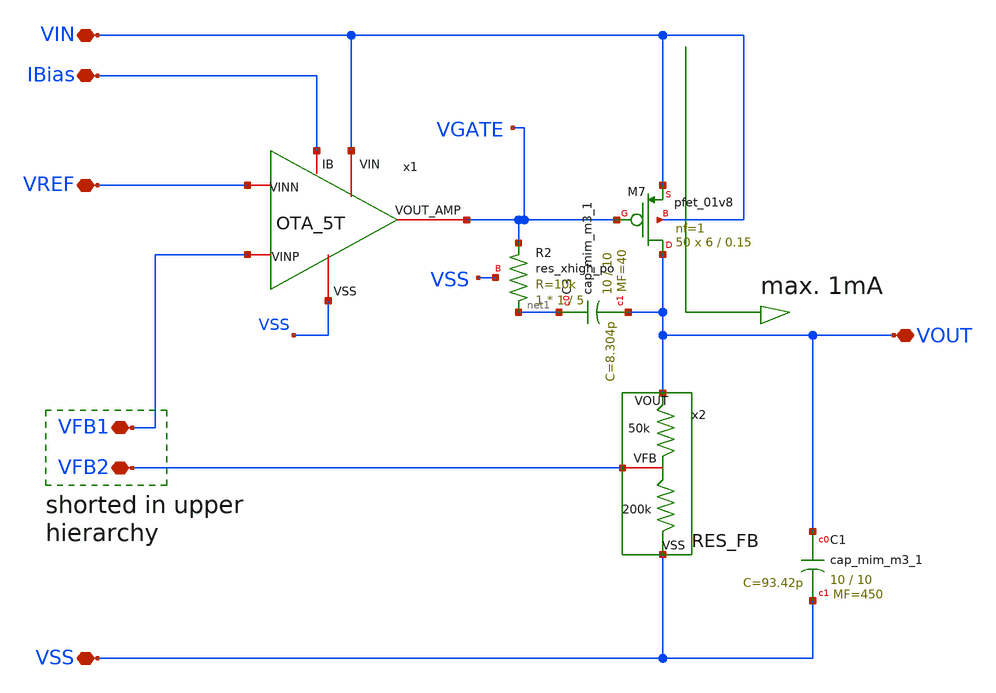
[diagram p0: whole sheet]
** sch_path: LDO_1p5V/schematics/LDO.sch
**.subckt LDO VIN VREF VFB1 VSS VFB2 VOUT IBias
*.iopin VIN
*.iopin VREF
*.iopin VFB1
*.iopin VSS
*.iopin VFB2
*.iopin VOUT
*.iopin IBias
x2 VOUT VFB2 VSS RES_FB
x1 VIN VGATE VREF VFB1 IBias VSS OTA_5T
XC3 net1 VOUT sky130_fd_pr__cap_mim_m3_1 W=10 L=10 MF=40 m=40
XM7 VOUT VGATE VIN VIN sky130_fd_pr__pfet_01v8 L=0.15 W=6 nf=1 ad='int((1 + 1)/2) * 6 / 1 * 0.29' as='int((1 + 2)/2) * 6 / 1 * 0.29'
+ pd='2*int((1 + 1)/2) * (6 / 1 + 0.29)' ps='2*int((1 + 2)/2) * (6 / 1 + 0.29)' nrd='0.29 / 6 ' nrs='0.29 / 6 '
+ sa=0 sb=0 sd=0 mult=50 m=50
XC1 VOUT VSS sky130_fd_pr__cap_mim_m3_1 W=10 L=10 MF=450 m=450
XR2 net1 VGATE VSS sky130_fd_pr__res_xhigh_po W=1 L=5 mult=1 m=1
**.ends

* expanding   symbol:  /foss/designs/IPN/LDO_1p5V/schematics/RES_FB.sym # of pins=3
** sym_path: RES_FB/RES_FB.sym
** sch_path: RES_FB/RES_FB.sch
.subckt RES_FB VOUT VFB VSS
*.iopin VOUT
*.iopin VFB
*.iopin VSS
XR11 net1 VOUT VSS sky130_fd_pr__res_xhigh_po_0p69 L=8.62 mult=1 m=1
XR1 VFB net1 VSS sky130_fd_pr__res_xhigh_po_0p69 L=8.62 mult=1 m=1
XR2 net8 VFB VSS sky130_fd_pr__res_xhigh_po_0p69 L=8.62 mult=1 m=1
XR3 net4 net8 VSS sky130_fd_pr__res_xhigh_po_0p69 L=8.62 mult=1 m=1
XR4 net2 net4 VSS sky130_fd_pr__res_xhigh_po_0p69 L=8.62 mult=1 m=1
XR5 net5 net2 VSS sky130_fd_pr__res_xhigh_po_0p69 L=8.62 mult=1 m=1
XR6 net3 net5 VSS sky130_fd_pr__res_xhigh_po_0p69 L=8.62 mult=1 m=1
XR7 net7 net3 VSS sky130_fd_pr__res_xhigh_po_0p69 L=8.62 mult=1 m=1
XR8 net6 net7 VSS sky130_fd_pr__res_xhigh_po_0p69 L=8.62 mult=1 m=1
XR9 VSS net6 VSS sky130_fd_pr__res_xhigh_po_0p69 L=8.62 mult=1 m=1
.ends


* expanding   symbol:  /foss/designs/IPN/LDO_1p5V/schematics/OTA_5T.sym # of pins=6
** sym_path: /foss/designs/IPN/LDO_1p5V/schematics/OTA_5T.sym
** sch_path: /foss/designs/IPN/LDO_1p5V/schematics/OTA_5T.sch
.subckt OTA_5T VIN VOUT_AMP VINN VINP IB VSS
*.iopin VIN
*.iopin VSS
*.iopin VOUT_AMP
*.iopin IB
*.iopin VINN
*.iopin VINP
XM1 IB IB VSS VSS sky130_fd_pr__nfet_01v8 L=1 W=2.5 nf=1 ad='int((1 + 1)/2) * 2.5 / 1 * 0.29' as='int((1 + 2)/2) * 2.5 / 1 * 0.29'
+ pd='2*int((1 + 1)/2) * (2.5 / 1 + 0.29)' ps='2*int((1 + 2)/2) * (2.5 / 1 + 0.29)' nrd='0.29 / 2.5 ' nrs='0.29 / 2.5 '
+ sa=0 sb=0 sd=0 mult=4 m=4
XM2 tail IB VSS VSS sky130_fd_pr__nfet_01v8 L=1 W=2.5 nf=1 ad='int((1 + 1)/2) * 2.5 / 1 * 0.29' as='int((1 + 2)/2) * 2.5 / 1 * 0.29'
+ pd='2*int((1 + 1)/2) * (2.5 / 1 + 0.29)' ps='2*int((1 + 2)/2) * (2.5 / 1 + 0.29)' nrd='0.29 / 2.5 ' nrs='0.29 / 2.5 '
+ sa=0 sb=0 sd=0 mult=4 m=4
XM5 VOUT_AMP net1 VIN VIN sky130_fd_pr__pfet_01v8 L=1 W=6 nf=1 ad='int((1 + 1)/2) * 6 / 1 * 0.29' as='int((1 + 2)/2) * 6 / 1 * 0.29'
+ pd='2*int((1 + 1)/2) * (6 / 1 + 0.29)' ps='2*int((1 + 2)/2) * (6 / 1 + 0.29)' nrd='0.29 / 6 ' nrs='0.29 / 6 '
+ sa=0 sb=0 sd=0 mult=4 m=4
XM6 net1 net1 VIN VIN sky130_fd_pr__pfet_01v8 L=1 W=6 nf=1 ad='int((1 + 1)/2) * 6 / 1 * 0.29' as='int((1 + 2)/2) * 6 / 1 * 0.29'
+ pd='2*int((1 + 1)/2) * (6 / 1 + 0.29)' ps='2*int((1 + 2)/2) * (6 / 1 + 0.29)' nrd='0.29 / 6 ' nrs='0.29 / 6 '
+ sa=0 sb=0 sd=0 mult=4 m=4
XD tail VSS tail VSS sky130_fd_pr__nfet_01v8 L=0.15 W=3 nf=1 ad='int((1 + 1)/2) * 3 / 1 * 0.29' as='int((1 + 2)/2) * 3 / 1 * 0.29'
+ pd='2*int((1 + 1)/2) * (3 / 1 + 0.29)' ps='2*int((1 + 2)/2) * (3 / 1 + 0.29)' nrd='0.29 / 3 ' nrs='0.29 / 3 '
+ sa=0 sb=0 sd=0 mult=4 m=4
XM7 VIN VIN VIN VIN sky130_fd_pr__pfet_01v8 L=0.15 W=6 nf=1 ad='int((1 + 1)/2) * 6 / 1 * 0.29' as='int((1 + 2)/2) * 6 / 1 * 0.29'
+ pd='2*int((1 + 1)/2) * (6 / 1 + 0.29)' ps='2*int((1 + 2)/2) * (6 / 1 + 0.29)' nrd='0.29 / 6 ' nrs='0.29 / 6 '
+ sa=0 sb=0 sd=0 mult=4 m=4
XM3 net1 VINP tail VSS sky130_fd_pr__nfet_01v8 L=1 W=3 nf=1 ad='int((1 + 1)/2) * 3 / 1 * 0.29' as='int((1 + 2)/2) * 3 / 1 * 0.29'
+ pd='2*int((1 + 1)/2) * (3 / 1 + 0.29)' ps='2*int((1 + 2)/2) * (3 / 1 + 0.29)' nrd='0.29 / 3 ' nrs='0.29 / 3 '
+ sa=0 sb=0 sd=0 mult=4 m=4
XM4 VOUT_AMP VINN tail VSS sky130_fd_pr__nfet_01v8 L=1 W=3 nf=1 ad='int((1 + 1)/2) * 3 / 1 * 0.29' as='int((1 + 2)/2) * 3 / 1 * 0.29'
+ pd='2*int((1 + 1)/2) * (3 / 1 + 0.29)' ps='2*int((1 + 2)/2) * (3 / 1 + 0.29)' nrd='0.29 / 3 ' nrs='0.29 / 3 '
+ sa=0 sb=0 sd=0 mult=4 m=4
.ends

.end
